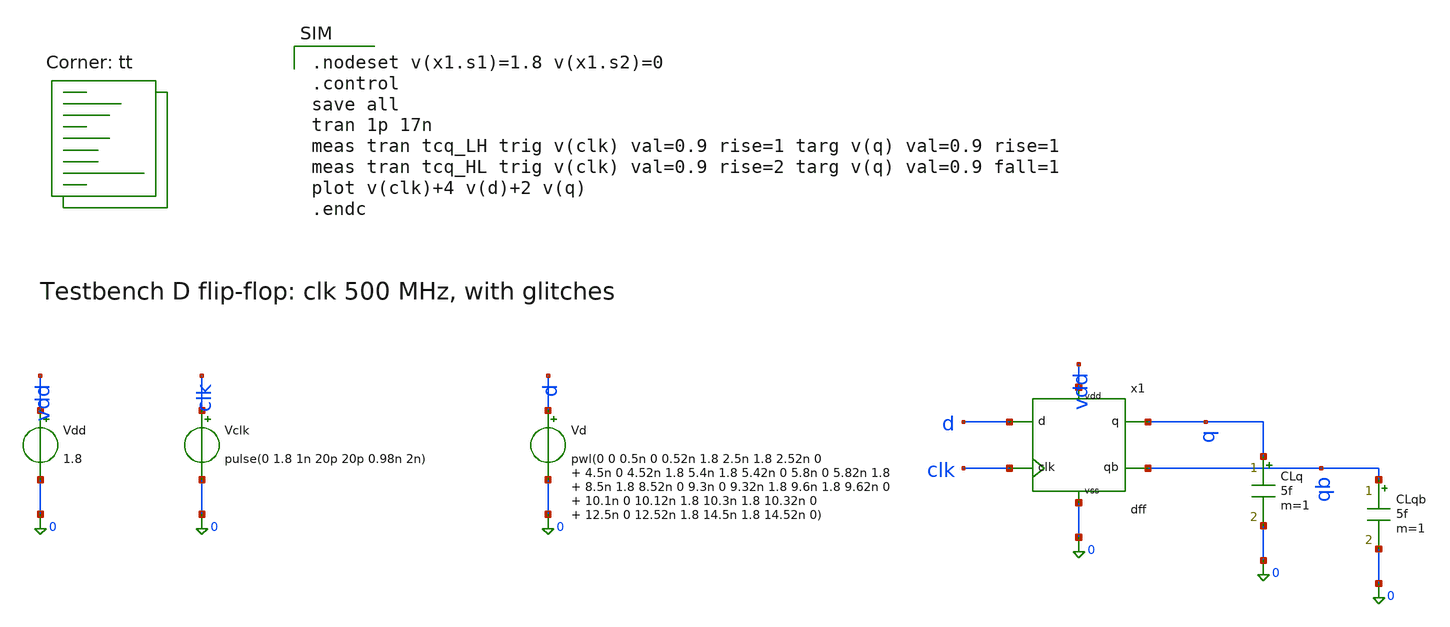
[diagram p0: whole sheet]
** sch_path: lab5/xschem/tb_dff.sch
**.subckt tb_dff
Vdd vdd 0 1.8
.save i(vdd)
Vclk clk 0 pulse(0 1.8 1n 20p 20p 0.98n 2n)
.save i(vclk)
Vd d 0 pwl(0 0 0.5n 0 0.52n 1.8 2.5n 1.8 2.52n 0 4.5n 0 4.52n 1.8 5.4n 1.8 5.42n 0 5.8n 0 5.82n 1.8
+ 8.5n 1.8 8.52n 0 9.3n 0 9.32n 1.8 9.6n 1.8 9.62n 0 10.1n 0 10.12n 1.8 10.3n 1.8 10.32n 0 12.5n 0 12.52n
+ 1.8 14.5n 1.8 14.52n 0)
.save i(vd)
x1 d clk q qb vdd 0 dff
CLq q 0 5f m=1
CLqb qb 0 5f m=1
**** begin user architecture code
.lib $::SKYWATER_MODELS/sky130.lib.spice tt

.nodeset v(x1.s1)=1.8 v(x1.s2)=0
.control
save all
tran 1p 17n
meas tran tcq_LH trig v(clk) val=0.9 rise=1 targ v(q) val=0.9 rise=1
meas tran tcq_HL trig v(clk) val=0.9 rise=2 targ v(q) val=0.9 fall=1
plot v(clk)+4 v(d)+2 v(q)
.endc

**** end user architecture code
**.ends
.end
